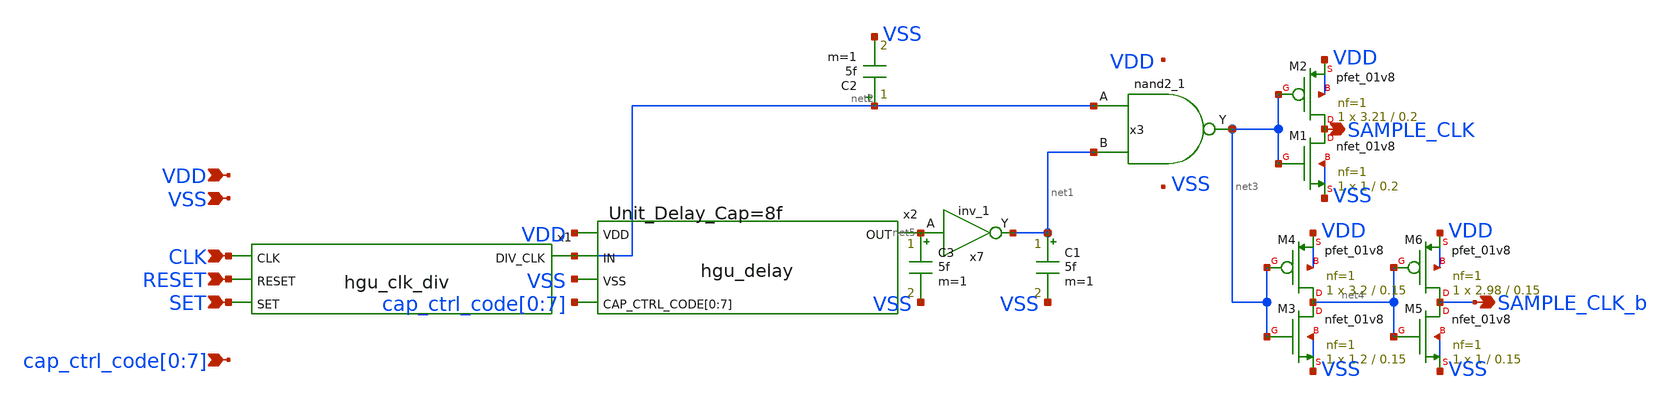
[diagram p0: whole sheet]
** sch_path: hgu/xschem/hgu_clk_sample.sch
**.subckt hgu_clk_sample VDD VSS SET RESET CLK SAMPLE_CLK
*+ cap_ctrl_code[0],cap_ctrl_code[1],cap_ctrl_code[2],cap_ctrl_code[3],cap_ctrl_code[4],cap_ctrl_code[5],cap_ctrl_code[6],cap_ctrl_code[7] SAMPLE_CLK_b
*.ipin VDD
*.ipin VSS
*.ipin SET
*.ipin RESET
*.ipin CLK
*.opin SAMPLE_CLK
*.ipin
*+ cap_ctrl_code[0],cap_ctrl_code[1],cap_ctrl_code[2],cap_ctrl_code[3],cap_ctrl_code[4],cap_ctrl_code[5],cap_ctrl_code[6],cap_ctrl_code[7]
*.opin SAMPLE_CLK_b
x1 net2 CLK RESET SET hgu_clk_div
x2 VDD net2 net5 VSS cap_ctrl_code[0] cap_ctrl_code[1] cap_ctrl_code[2] cap_ctrl_code[3]
+ cap_ctrl_code[4] cap_ctrl_code[5] cap_ctrl_code[6] cap_ctrl_code[7] hgu_delay DELAY_CAP=8f
x7 net5 VGND VNB VPB VPWR net1 sky130_fd_sc_hd__inv_1
C1 net1 VSS 5f m=1
C2 net2 VSS 5f m=1
C3 net5 VSS 5f m=1
x3 net2 net1 VGND VNB VPB VPWR net3 sky130_fd_sc_hd__nand2_1
XM1 SAMPLE_CLK net3 VSS VSS sky130_fd_pr__nfet_01v8 L=0.2 W=1 nf=1 ad='int((nf+1)/2) * W/nf * 0.29' as='int((nf+2)/2) * W/nf * 0.29'
+ pd='2*int((nf+1)/2) * (W/nf + 0.29)' ps='2*int((nf+2)/2) * (W/nf + 0.29)' nrd='0.29 / W' nrs='0.29 / W'
+ sa=0 sb=0 sd=0 mult=1 m=1
XM2 SAMPLE_CLK net3 VDD VDD sky130_fd_pr__pfet_01v8 L=0.2 W=3.21 nf=1 ad='int((nf+1)/2) * W/nf * 0.29'
+ as='int((nf+2)/2) * W/nf * 0.29' pd='2*int((nf+1)/2) * (W/nf + 0.29)' ps='2*int((nf+2)/2) * (W/nf + 0.29)'
+ nrd='0.29 / W' nrs='0.29 / W' sa=0 sb=0 sd=0 mult=1 m=1
XM3 net4 net3 VSS VSS sky130_fd_pr__nfet_01v8 L=0.15 W=1.2 nf=1 ad='int((nf+1)/2) * W/nf * 0.29' as='int((nf+2)/2) * W/nf * 0.29'
+ pd='2*int((nf+1)/2) * (W/nf + 0.29)' ps='2*int((nf+2)/2) * (W/nf + 0.29)' nrd='0.29 / W' nrs='0.29 / W'
+ sa=0 sb=0 sd=0 mult=1 m=1
XM4 net4 net3 VDD VDD sky130_fd_pr__pfet_01v8 L=0.15 W=3.2 nf=1 ad='int((nf+1)/2) * W/nf * 0.29' as='int((nf+2)/2) * W/nf * 0.29'
+ pd='2*int((nf+1)/2) * (W/nf + 0.29)' ps='2*int((nf+2)/2) * (W/nf + 0.29)' nrd='0.29 / W' nrs='0.29 / W'
+ sa=0 sb=0 sd=0 mult=1 m=1
XM5 SAMPLE_CLK_b net4 VSS VSS sky130_fd_pr__nfet_01v8 L=0.15 W=1 nf=1 ad='int((nf+1)/2) * W/nf * 0.29'
+ as='int((nf+2)/2) * W/nf * 0.29' pd='2*int((nf+1)/2) * (W/nf + 0.29)' ps='2*int((nf+2)/2) * (W/nf + 0.29)'
+ nrd='0.29 / W' nrs='0.29 / W' sa=0 sb=0 sd=0 mult=1 m=1
XM6 SAMPLE_CLK_b net4 VDD VDD sky130_fd_pr__pfet_01v8 L=0.15 W=2.98 nf=1 ad='int((nf+1)/2) * W/nf * 0.29'
+ as='int((nf+2)/2) * W/nf * 0.29' pd='2*int((nf+1)/2) * (W/nf + 0.29)' ps='2*int((nf+2)/2) * (W/nf + 0.29)'
+ nrd='0.29 / W' nrs='0.29 / W' sa=0 sb=0 sd=0 mult=1 m=1
**.ends
.end
